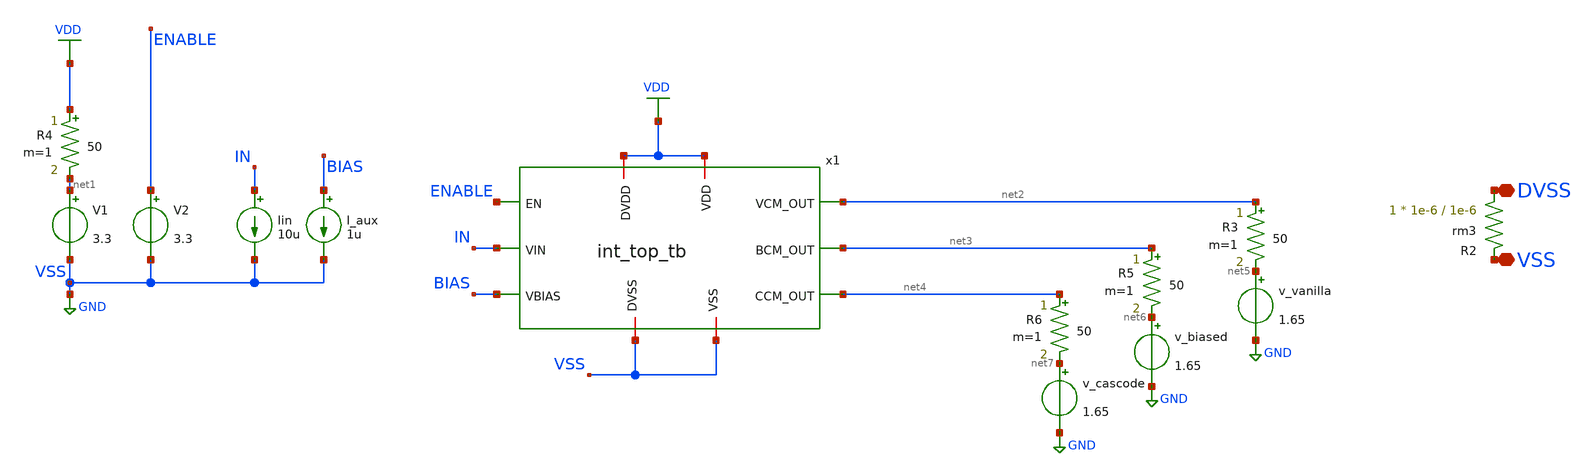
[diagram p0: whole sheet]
** sch_path: blocks/composite/regulated_cascoded_cmirror/xschem/chip_top.sch
**.subckt chip_top DVSS VSS
*.iopin DVSS
*.iopin VSS
XR2 DVSS VSS rm3 r_width=1e-6 r_length=1e-6 m=1
v_vanilla net5 GND 1.65
.save i(v_vanilla)
v_biased net6 GND 1.65
.save i(v_biased)
v_cascode net7 GND 1.65
.save i(v_cascode)
R3 net2 net5 50 m=1
R5 net3 net6 50 m=1
R6 net4 net7 50 m=1
V1 net1 GND 3.3
R4 VDD net1 50 m=1
x1 net2 ENABLE net3 net4 IN VSS VDD VDD VSS BIAS int_top_tb
V2 ENABLE GND 3.3
Iin IN GND 10u
I_aux BIAS GND 1u
**** begin user architecture code

.include /foss/designs/gLayout-mahowalders/blocks/composite/regulated_cascoded_cmirror/xschem/Chipathon2025_pads/xschem/gf180mcu_fd_io.spice
.include /foss/designs/gLayout-mahowalders/blocks/composite/regulated_cascoded_cmirror/xschem/Chipathon2025_pads/xschem/gf180mcu_fd_io__asig_5p0_extracted.spice
.include /foss/pdks/gf180mcuD/libs.tech/ngspice/design.ngspice
.lib /foss/pdks/gf180mcuD/libs.tech/ngspice/sm141064.ngspice typical
.lib /foss/pdks/gf180mcuD/libs.tech/ngspice/sm141064.ngspice diode_typical
.lib /foss/pdks/gf180mcuD/libs.tech/ngspice/sm141064.ngspice res_typical
.lib /foss/pdks/gf180mcuD/libs.tech/ngspice/sm141064.ngspice moscap_typical
.lib /foss/pdks/gf180mcuD/libs.tech/ngspice/sm141064.ngspice mimcap_typical



.options savecurrents
.param temp=27
.control
set wr_singlescale
set noaskquit
*set appendwrite
set hcopypscolor=1

save all
op
write tb_vcm.raw
* --- Run vanilla sweep ---
dc v_vanilla 0 3.3 0.01
let i_vanilla = -i(v_vanilla)
wrdata vanilla.txt i_vanilla
write tb_vcm.raw
* --- Run biased sweep ---
reset
write tb_bcm.raw
dc v_biased 0 3.3 0.01
let i_biased = -i(v_biased)
wrdata biased.txt i_biased
write tb_bcm.raw
* --- Run cascode sweep ---
reset
write tb_ccm.raw
dc v_cascode 0 3.3 0.01 I_aux 1u 10u 100n
let i_cascode = -i(v_cascode)
wrdata cascode.txt i_cascode
write tb_ccm.raw
.endc


**** end user architecture code
**.ends
.GLOBAL GND
.GLOBAL VDD
.end
